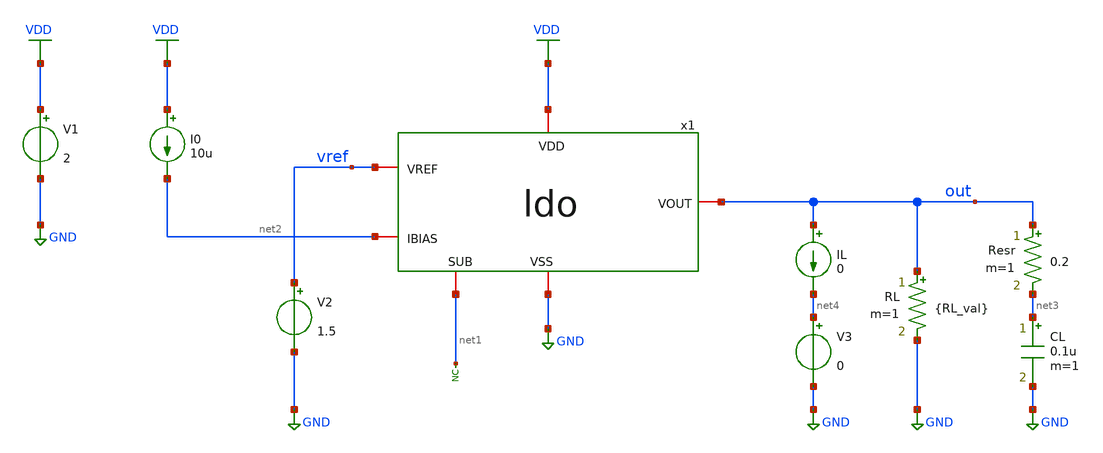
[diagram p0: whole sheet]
** sch_path: designs/libs/tb_ldo/tb_ldo/tb_ldo/tb_ldo_tran/tb_ldo_tran.sch
**.subckt tb_ldo_tran
* noconn #net1
RL out GND {RL_val} m=1
V1 VDD GND 2
V2 vref GND 1.5
I0 VDD net2 10u
CL net3 GND 0.1u m=1
Resr out net3 0.2 m=1
x1 VDD vref out net2 net1 GND ldo
IL out net4 0
V3 net4 GND 0
**** begin user architecture code



.control
save all

** Define params
.param RL_val = 1.8k

** Define input signal
let fsig = 1k
let tper = 1/fsig
let tfr1 = 10u
let ton1 = 0.5*tper-2*tfr1
let td1 = 10u
let tfr2 = 1u
let ton2 = 0.5*tper-2*tfr2
let td2 = 2u

** Define transient params
let tstop1 = 50u
let tstep1 = 0.01u
let tstop2 = 10u
let tstep2 = 100n

** Transient response to Vdd ramp simulation
alter @V1[PULSE] = [ 0 2 $&td1 $&tfr1 $&tfr1 $&ton1 $&tper 0 ]
alter RL = {RL_val}
alter @IL[PULSE] = [ 0 0 $&td1 $&tfr1 $&tfr1 $&ton1 $&tper 0 ]
tran $&tstep1 $&tstop1

** Plots
setplot tran1
let vout = v(out)
let vin = v(vdd)
plot vout
plot vin

write tb_ldo_tran1.raw

** Transient response to Iload ramp simulation
alter @V1[PULSE] = [ 2 2 $&td2 $&tfr2 $&tfr2 $&ton2 $&tper2 0 ]
alter RL = 1e15
alter @IL[PULSE] = [ 0 1m $&td2 $&tfr2 $&tfr2 $&ton2 $&tper 0 ]
tran $&tstep2 $&tstop2

** Plots
setplot tran2
let vout = v(out)
let iload = v3#branch
plot iload
plot vout

write tb_ldo_tran2.raw

** LDO Functional transient simulation
alter @V1[PULSE] = [ 3.3 2 0 1u 1u 248u 500u 0 ]
alter RL = {RL_val}
alter @IL[PULSE] = [ 0 0 0 1u 1u 248u 500u 0 ]
tran 0.5u 500u

** Plots
setplot tran3
let vin = v(vdd)
let vota = v(x1.vota)
let vout = v(out)
plot vin vout vota

write tb_ldo_tran3.raw

.endc
* ngspice commands




.include $::180MCU_MODELS/design.ngspice
.lib $::180MCU_MODELS/sm141064.ngspice typical
.lib $::180MCU_MODELS/sm141064.ngspice cap_mim
.lib $::180MCU_MODELS/sm141064.ngspice moscap_typical
.lib $::180MCU_MODELS/sm141064.ngspice mimcap_typical
.lib $::180MCU_MODELS/sm141064.ngspice res_typical
* .lib $::180MCU_MODELS/sm141064.ngspice res_statistical
* ngspice commands

**** end user architecture code
**.ends
.GLOBAL GND
.GLOBAL VDD
.end
